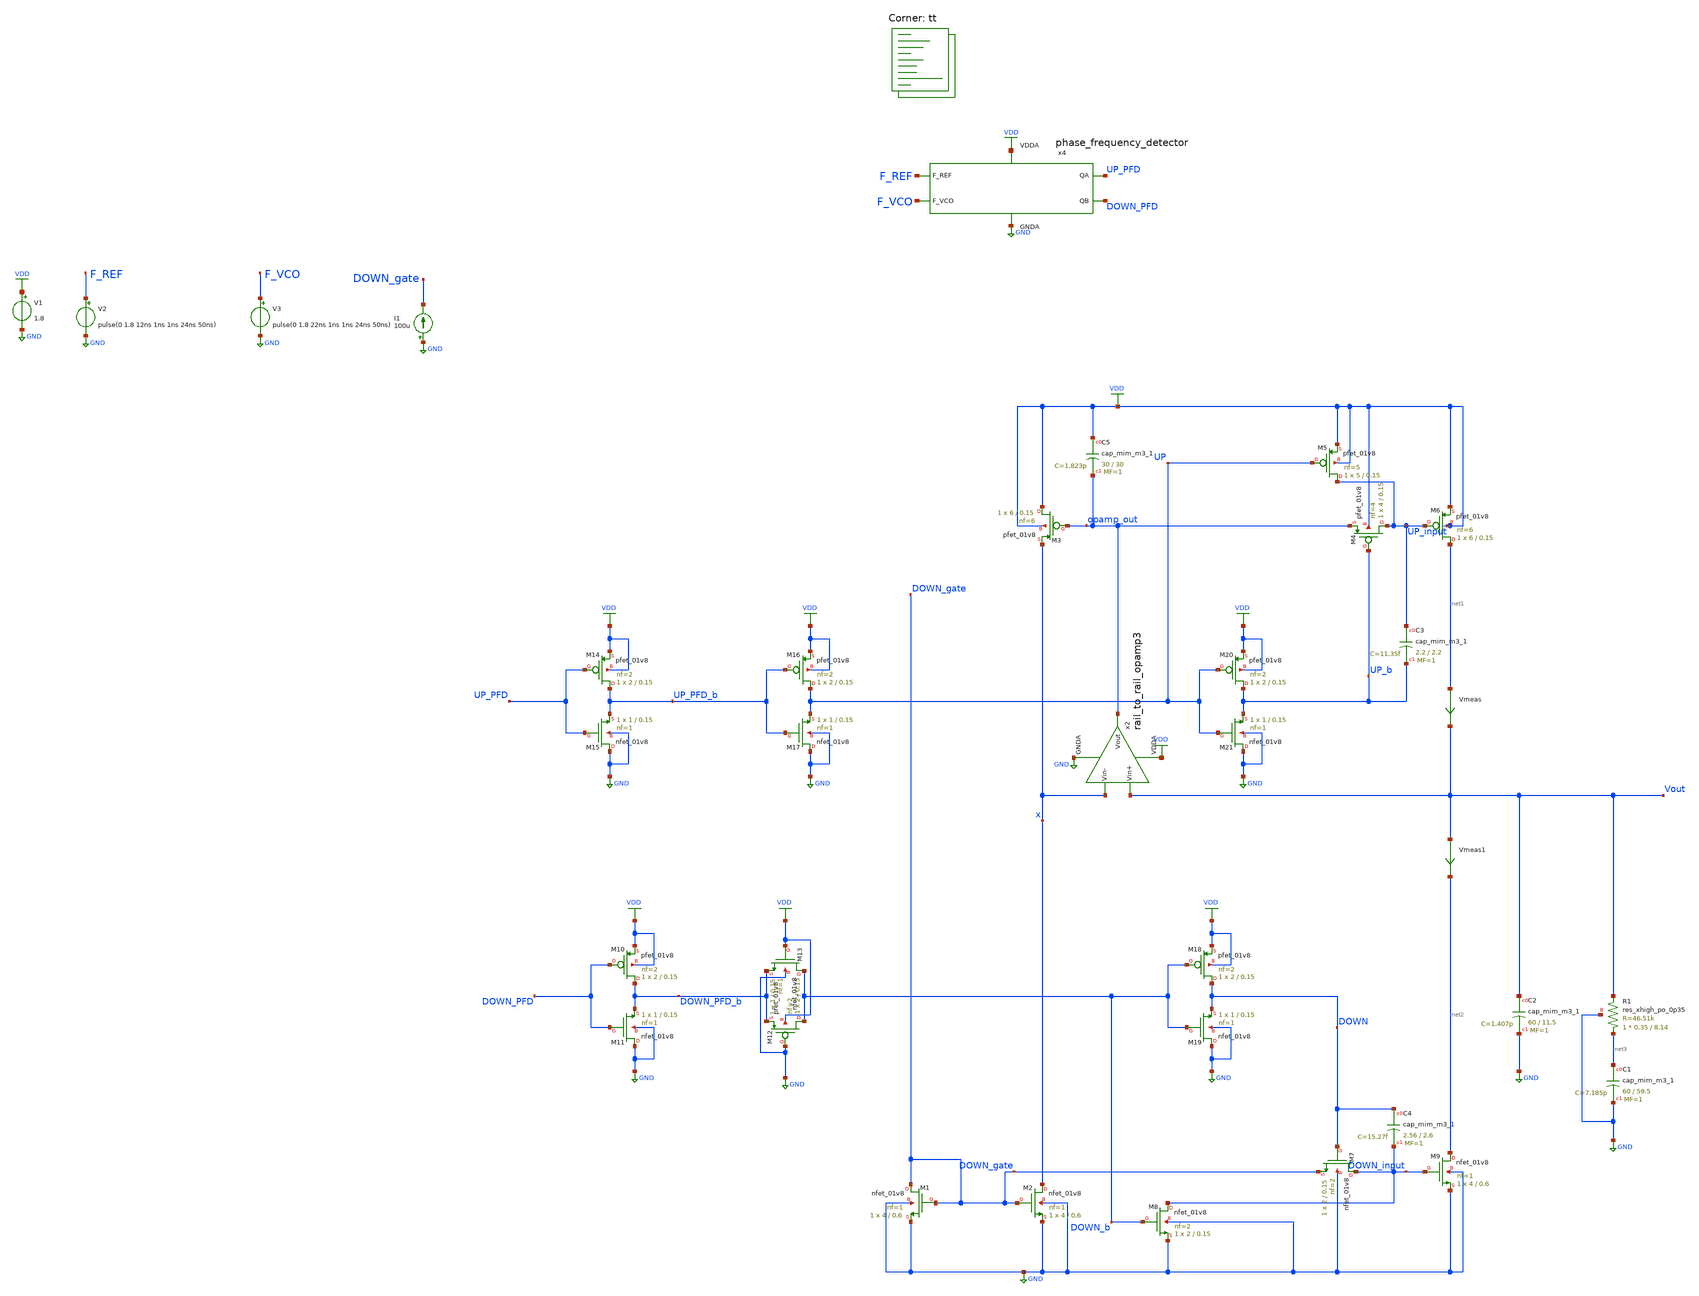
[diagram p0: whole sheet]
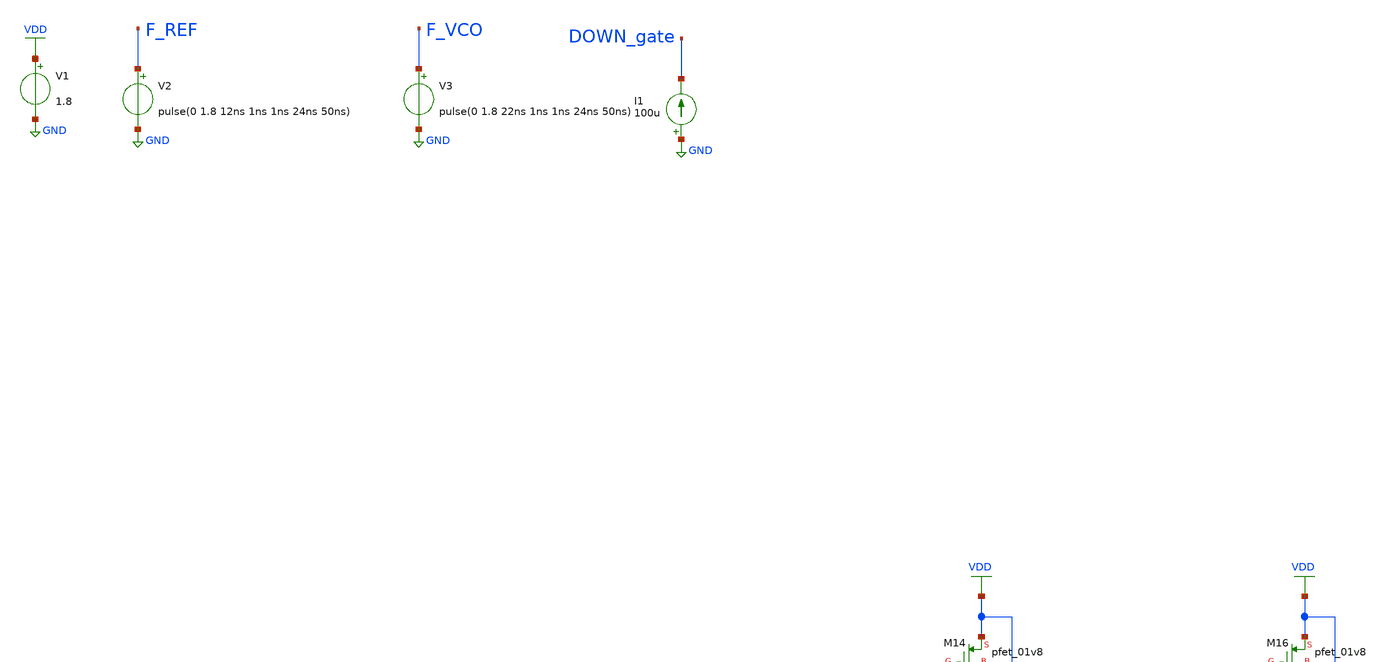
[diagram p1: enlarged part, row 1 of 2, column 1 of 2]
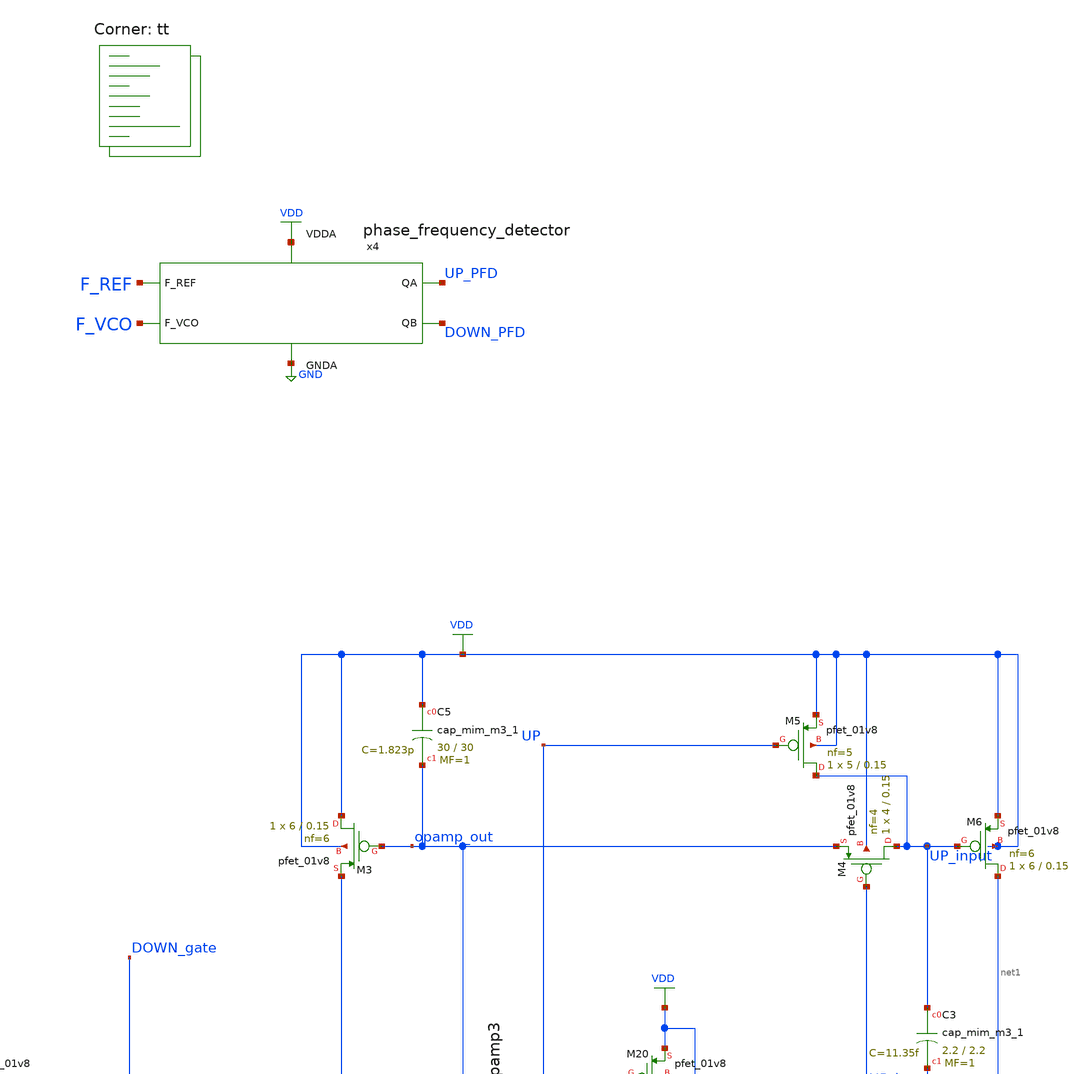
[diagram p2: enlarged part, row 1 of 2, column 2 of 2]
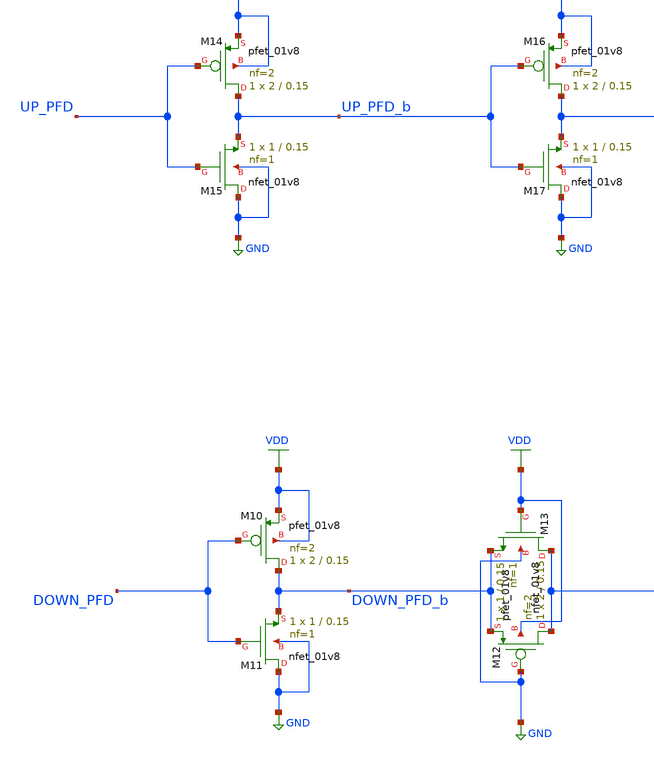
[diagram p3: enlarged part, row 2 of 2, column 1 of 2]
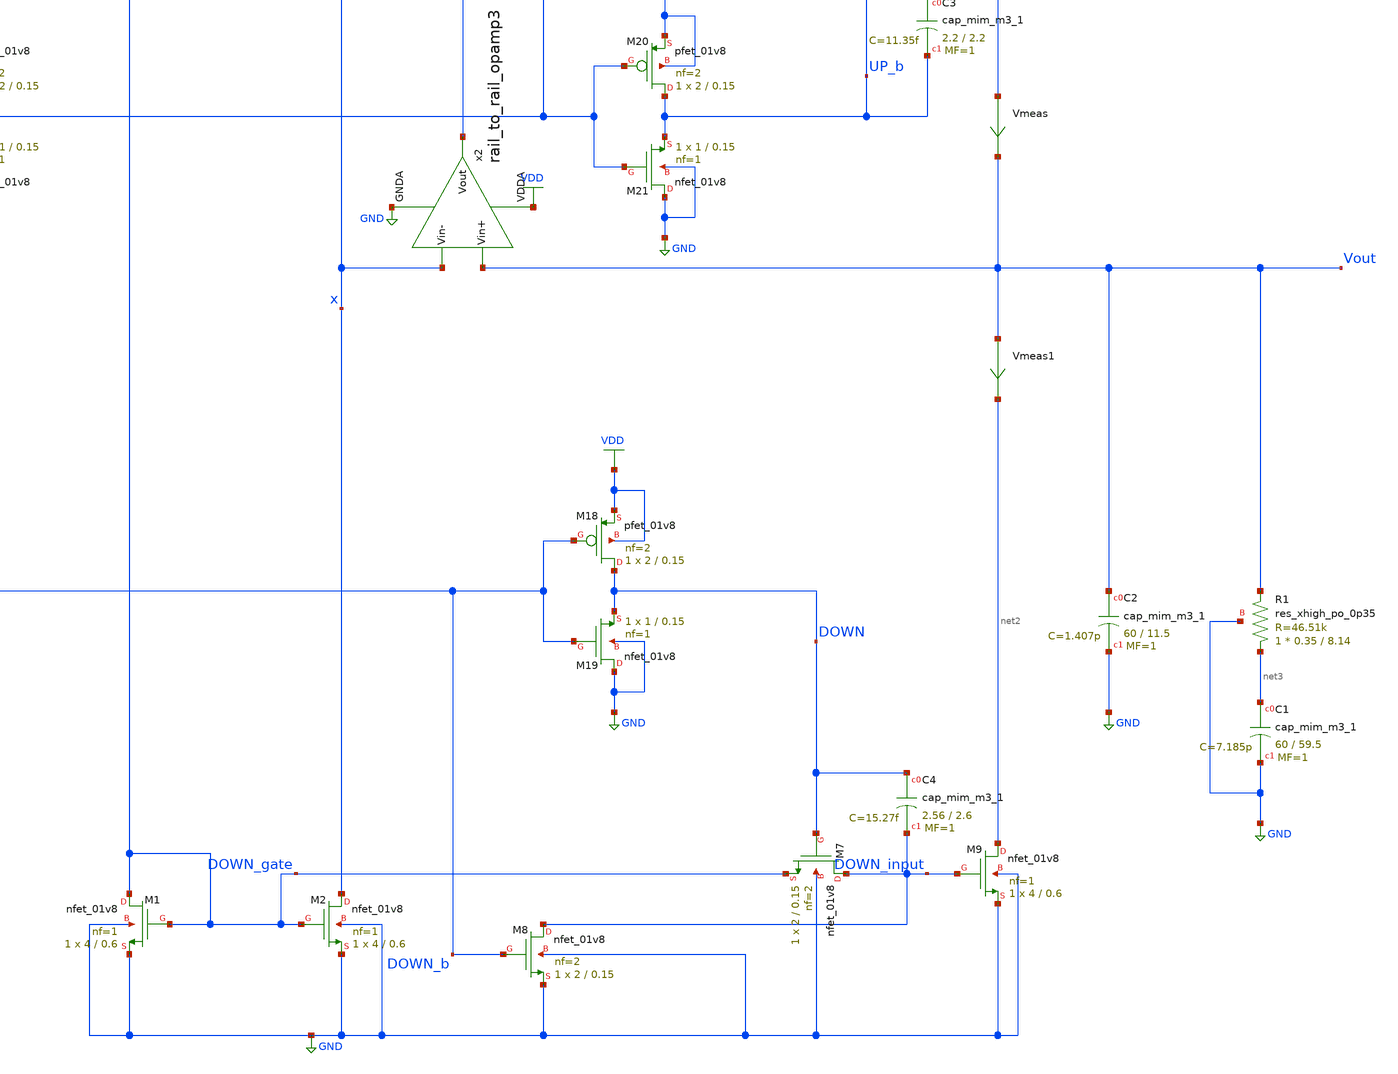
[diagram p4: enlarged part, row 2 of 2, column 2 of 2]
** sch_path: projects/pll/charge_pump/xschem_ngspice/pfd_charge_pump_8.sch
**.subckt pfd_charge_pump_8
XM1 DOWN_gate DOWN_gate GND GND sky130_fd_pr__nfet_01v8 L=0.6 W=4 nf=1 ad='int((nf+1)/2) * W/nf * 0.29'
+ as='int((nf+2)/2) * W/nf * 0.29' pd='2*int((nf+1)/2) * (W/nf + 0.29)' ps='2*int((nf+2)/2) * (W/nf + 0.29)'
+ nrd='0.29 / W' nrs='0.29 / W' sa=0 sb=0 sd=0 mult=1 m=1
XM2 x DOWN_gate GND GND sky130_fd_pr__nfet_01v8 L=0.6 W=4 nf=1 ad='int((nf+1)/2) * W/nf * 0.29' as='int((nf+2)/2) * W/nf * 0.29'
+ pd='2*int((nf+1)/2) * (W/nf + 0.29)' ps='2*int((nf+2)/2) * (W/nf + 0.29)' nrd='0.29 / W' nrs='0.29 / W'
+ sa=0 sb=0 sd=0 mult=1 m=1
XM3 VDD opamp_out x VDD sky130_fd_pr__pfet_01v8 L=0.15 W=6 nf=6 ad='int((nf+1)/2) * W/nf * 0.29' as='int((nf+2)/2) * W/nf * 0.29'
+ pd='2*int((nf+1)/2) * (W/nf + 0.29)' ps='2*int((nf+2)/2) * (W/nf + 0.29)' nrd='0.29 / W' nrs='0.29 / W'
+ sa=0 sb=0 sd=0 mult=1 m=1
V1 VDD GND 1.8
XM4 UP_input UP_b opamp_out VDD sky130_fd_pr__pfet_01v8 L=0.15 W=4 nf=4 ad='int((nf+1)/2) * W/nf * 0.29'
+ as='int((nf+2)/2) * W/nf * 0.29' pd='2*int((nf+1)/2) * (W/nf + 0.29)' ps='2*int((nf+2)/2) * (W/nf + 0.29)'
+ nrd='0.29 / W' nrs='0.29 / W' sa=0 sb=0 sd=0 mult=1 m=1
XM5 UP_input UP VDD VDD sky130_fd_pr__pfet_01v8 L=0.15 W=5 nf=5 ad='int((nf+1)/2) * W/nf * 0.29' as='int((nf+2)/2) * W/nf * 0.29'
+ pd='2*int((nf+1)/2) * (W/nf + 0.29)' ps='2*int((nf+2)/2) * (W/nf + 0.29)' nrd='0.29 / W' nrs='0.29 / W'
+ sa=0 sb=0 sd=0 mult=1 m=1
XM6 net1 UP_input VDD VDD sky130_fd_pr__pfet_01v8 L=0.15 W=6 nf=6 ad='int((nf+1)/2) * W/nf * 0.29' as='int((nf+2)/2) * W/nf * 0.29'
+ pd='2*int((nf+1)/2) * (W/nf + 0.29)' ps='2*int((nf+2)/2) * (W/nf + 0.29)' nrd='0.29 / W' nrs='0.29 / W'
+ sa=0 sb=0 sd=0 mult=1 m=1
XM7 DOWN_input DOWN DOWN_gate GND sky130_fd_pr__nfet_01v8 L=0.15 W=2 nf=2 ad='int((nf+1)/2) * W/nf * 0.29'
+ as='int((nf+2)/2) * W/nf * 0.29' pd='2*int((nf+1)/2) * (W/nf + 0.29)' ps='2*int((nf+2)/2) * (W/nf + 0.29)'
+ nrd='0.29 / W' nrs='0.29 / W' sa=0 sb=0 sd=0 mult=1 m=1
XM8 DOWN_input DOWN_b GND GND sky130_fd_pr__nfet_01v8 L=0.15 W=2 nf=2 ad='int((nf+1)/2) * W/nf * 0.29'
+ as='int((nf+2)/2) * W/nf * 0.29' pd='2*int((nf+1)/2) * (W/nf + 0.29)' ps='2*int((nf+2)/2) * (W/nf + 0.29)'
+ nrd='0.29 / W' nrs='0.29 / W' sa=0 sb=0 sd=0 mult=1 m=1
XM9 net2 DOWN_input GND GND sky130_fd_pr__nfet_01v8 L=0.6 W=4 nf=1 ad='int((nf+1)/2) * W/nf * 0.29' as='int((nf+2)/2) * W/nf * 0.29'
+ pd='2*int((nf+1)/2) * (W/nf + 0.29)' ps='2*int((nf+2)/2) * (W/nf + 0.29)' nrd='0.29 / W' nrs='0.29 / W'
+ sa=0 sb=0 sd=0 mult=1 m=1
XC2 Vout GND sky130_fd_pr__cap_mim_m3_1 W=60 L=11.5 MF=1 m=1
XC1 net3 GND sky130_fd_pr__cap_mim_m3_1 W=60 L=59.5 MF=1 m=1
V2 F_REF GND pulse(0 1.8 12ns 1ns 1ns 24ns 50ns)
V3 F_VCO GND pulse(0 1.8 22ns 1ns 1ns 24ns 50ns)
x4 F_REF F_VCO VDD UP_PFD DOWN_PFD GND phase_frequency_detector
x2 VDD Vout x opamp_out GND rail_to_rail_opamp3
XR1 net3 Vout GND sky130_fd_pr__res_xhigh_po_0p35 L=8.14 mult=1 m=1
XM12 DOWN_b GND DOWN_PFD_b VDD sky130_fd_pr__pfet_01v8 L=0.15 W=2 nf=2 ad='int((nf+1)/2) * W/nf * 0.29'
+ as='int((nf+2)/2) * W/nf * 0.29' pd='2*int((nf+1)/2) * (W/nf + 0.29)' ps='2*int((nf+2)/2) * (W/nf + 0.29)'
+ nrd='0.29 / W' nrs='0.29 / W' sa=0 sb=0 sd=0 mult=1 m=1
XM13 DOWN_b VDD DOWN_PFD_b GND sky130_fd_pr__nfet_01v8 L=0.15 W=1 nf=1 ad='int((nf+1)/2) * W/nf * 0.29'
+ as='int((nf+2)/2) * W/nf * 0.29' pd='2*int((nf+1)/2) * (W/nf + 0.29)' ps='2*int((nf+2)/2) * (W/nf + 0.29)'
+ nrd='0.29 / W' nrs='0.29 / W' sa=0 sb=0 sd=0 mult=1 m=1
XC5 VDD opamp_out sky130_fd_pr__cap_mim_m3_1 W=30 L=30 MF=1 m=1
XM10 DOWN_PFD_b DOWN_PFD VDD VDD sky130_fd_pr__pfet_01v8 L=0.15 W=2 nf=2 ad='int((nf+1)/2) * W/nf * 0.29'
+ as='int((nf+2)/2) * W/nf * 0.29' pd='2*int((nf+1)/2) * (W/nf + 0.29)' ps='2*int((nf+2)/2) * (W/nf + 0.29)'
+ nrd='0.29 / W' nrs='0.29 / W' sa=0 sb=0 sd=0 mult=1 m=1
XM11 GND DOWN_PFD DOWN_PFD_b GND sky130_fd_pr__nfet_01v8 L=0.15 W=1 nf=1 ad='int((nf+1)/2) * W/nf * 0.29'
+ as='int((nf+2)/2) * W/nf * 0.29' pd='2*int((nf+1)/2) * (W/nf + 0.29)' ps='2*int((nf+2)/2) * (W/nf + 0.29)'
+ nrd='0.29 / W' nrs='0.29 / W' sa=0 sb=0 sd=0 mult=1 m=1
XM14 UP_PFD_b UP_PFD VDD VDD sky130_fd_pr__pfet_01v8 L=0.15 W=2 nf=2 ad='int((nf+1)/2) * W/nf * 0.29'
+ as='int((nf+2)/2) * W/nf * 0.29' pd='2*int((nf+1)/2) * (W/nf + 0.29)' ps='2*int((nf+2)/2) * (W/nf + 0.29)'
+ nrd='0.29 / W' nrs='0.29 / W' sa=0 sb=0 sd=0 mult=1 m=1
XM15 GND UP_PFD UP_PFD_b GND sky130_fd_pr__nfet_01v8 L=0.15 W=1 nf=1 ad='int((nf+1)/2) * W/nf * 0.29'
+ as='int((nf+2)/2) * W/nf * 0.29' pd='2*int((nf+1)/2) * (W/nf + 0.29)' ps='2*int((nf+2)/2) * (W/nf + 0.29)'
+ nrd='0.29 / W' nrs='0.29 / W' sa=0 sb=0 sd=0 mult=1 m=1
XM16 UP UP_PFD_b VDD VDD sky130_fd_pr__pfet_01v8 L=0.15 W=2 nf=2 ad='int((nf+1)/2) * W/nf * 0.29' as='int((nf+2)/2) * W/nf * 0.29'
+ pd='2*int((nf+1)/2) * (W/nf + 0.29)' ps='2*int((nf+2)/2) * (W/nf + 0.29)' nrd='0.29 / W' nrs='0.29 / W'
+ sa=0 sb=0 sd=0 mult=1 m=1
XM17 GND UP_PFD_b UP GND sky130_fd_pr__nfet_01v8 L=0.15 W=1 nf=1 ad='int((nf+1)/2) * W/nf * 0.29' as='int((nf+2)/2) * W/nf * 0.29'
+ pd='2*int((nf+1)/2) * (W/nf + 0.29)' ps='2*int((nf+2)/2) * (W/nf + 0.29)' nrd='0.29 / W' nrs='0.29 / W'
+ sa=0 sb=0 sd=0 mult=1 m=1
XM18 DOWN DOWN_b VDD VDD sky130_fd_pr__pfet_01v8 L=0.15 W=2 nf=2 ad='int((nf+1)/2) * W/nf * 0.29' as='int((nf+2)/2) * W/nf * 0.29'
+ pd='2*int((nf+1)/2) * (W/nf + 0.29)' ps='2*int((nf+2)/2) * (W/nf + 0.29)' nrd='0.29 / W' nrs='0.29 / W'
+ sa=0 sb=0 sd=0 mult=1 m=1
XM19 GND DOWN_b DOWN GND sky130_fd_pr__nfet_01v8 L=0.15 W=1 nf=1 ad='int((nf+1)/2) * W/nf * 0.29' as='int((nf+2)/2) * W/nf * 0.29'
+ pd='2*int((nf+1)/2) * (W/nf + 0.29)' ps='2*int((nf+2)/2) * (W/nf + 0.29)' nrd='0.29 / W' nrs='0.29 / W'
+ sa=0 sb=0 sd=0 mult=1 m=1
XM20 UP_b UP VDD VDD sky130_fd_pr__pfet_01v8 L=0.15 W=2 nf=2 ad='int((nf+1)/2) * W/nf * 0.29' as='int((nf+2)/2) * W/nf * 0.29'
+ pd='2*int((nf+1)/2) * (W/nf + 0.29)' ps='2*int((nf+2)/2) * (W/nf + 0.29)' nrd='0.29 / W' nrs='0.29 / W'
+ sa=0 sb=0 sd=0 mult=1 m=1
XM21 GND UP UP_b GND sky130_fd_pr__nfet_01v8 L=0.15 W=1 nf=1 ad='int((nf+1)/2) * W/nf * 0.29' as='int((nf+2)/2) * W/nf * 0.29'
+ pd='2*int((nf+1)/2) * (W/nf + 0.29)' ps='2*int((nf+2)/2) * (W/nf + 0.29)' nrd='0.29 / W' nrs='0.29 / W'
+ sa=0 sb=0 sd=0 mult=1 m=1
I1 GND DOWN_gate 100u
Vmeas net1 Vout 0
.save i(vmeas)
Vmeas1 Vout net2 0
.save i(vmeas1)
XC3 UP_input UP_b sky130_fd_pr__cap_mim_m3_1 W=2.2 L=2.2 MF=1 m=1
XC4 DOWN DOWN_input sky130_fd_pr__cap_mim_m3_1 W=2.56 L=2.6 MF=1 m=1
**** begin user architecture code
.lib $::SKYWATER_MODELS/sky130.lib.spice tt



.include /foss/pdks/sky130A/libs.ref/sky130_fd_sc_hd/spice/sky130_fd_sc_hd.spice

.option method=gear
.option wnflag=1
* .option savecurrents

* .temp = 75

* .ic v(vout) = 1.8
* .ic v(vout) = 0.875
.ic v(vout) = 0.9

.save  v(up_pfd) v(down_pfd) v(up_pfd_b) v(down_pfd_b) v(up) v(up_b) v(down) v(down_b) v(v2) v(x) v(y) v(z) v(vout) v(up_input) v(down_input) v(down_gate) v(opamp_out) v(x2.p_bias) v(x2.n_bias) v(x2.v_common_p) v(x2.v_common_n) v(x2.p_left) v(x2.p_right) v(x2.n_left) v(x2.n_right) v(f_ref) v(f_vco) v(x4.qa) v(x4.qa_b) v(x4.qb) v(x4.qb_b) v(x4.qa) v(x4.e) v(x4.e_b) v(x4.f) v(x4.f_b) v(x4.before_reset) v(x4.reset) @m.xm6.msky130_fd_pr__pfet_01v8[id] @m.xm9.msky130_fd_pr__nfet_01v8[id]


.control
  * save v(up_pfd) v(down_pfd) v(up_pfd_b) v(down_pfd_b) v(up) v(up_b) v(down) v(down_b) v(x)
+ v(vout) v(up_input) v(down_input)
  * save all

  tran 50ps 0.5us
  * dc v2 0 1.8 0.01
  remzerovec
  write pfd_charge_pump_8_2.raw
  * wrdata /foss/designs/my_design/projects/pll/charge_pump/xschem_ngspice/pfd_charge_pump_7_QA.txt
+ v(osc)
  set appendwrite

.endc






**** end user architecture code
**.ends
.GLOBAL VDD
.GLOBAL GND
.end
